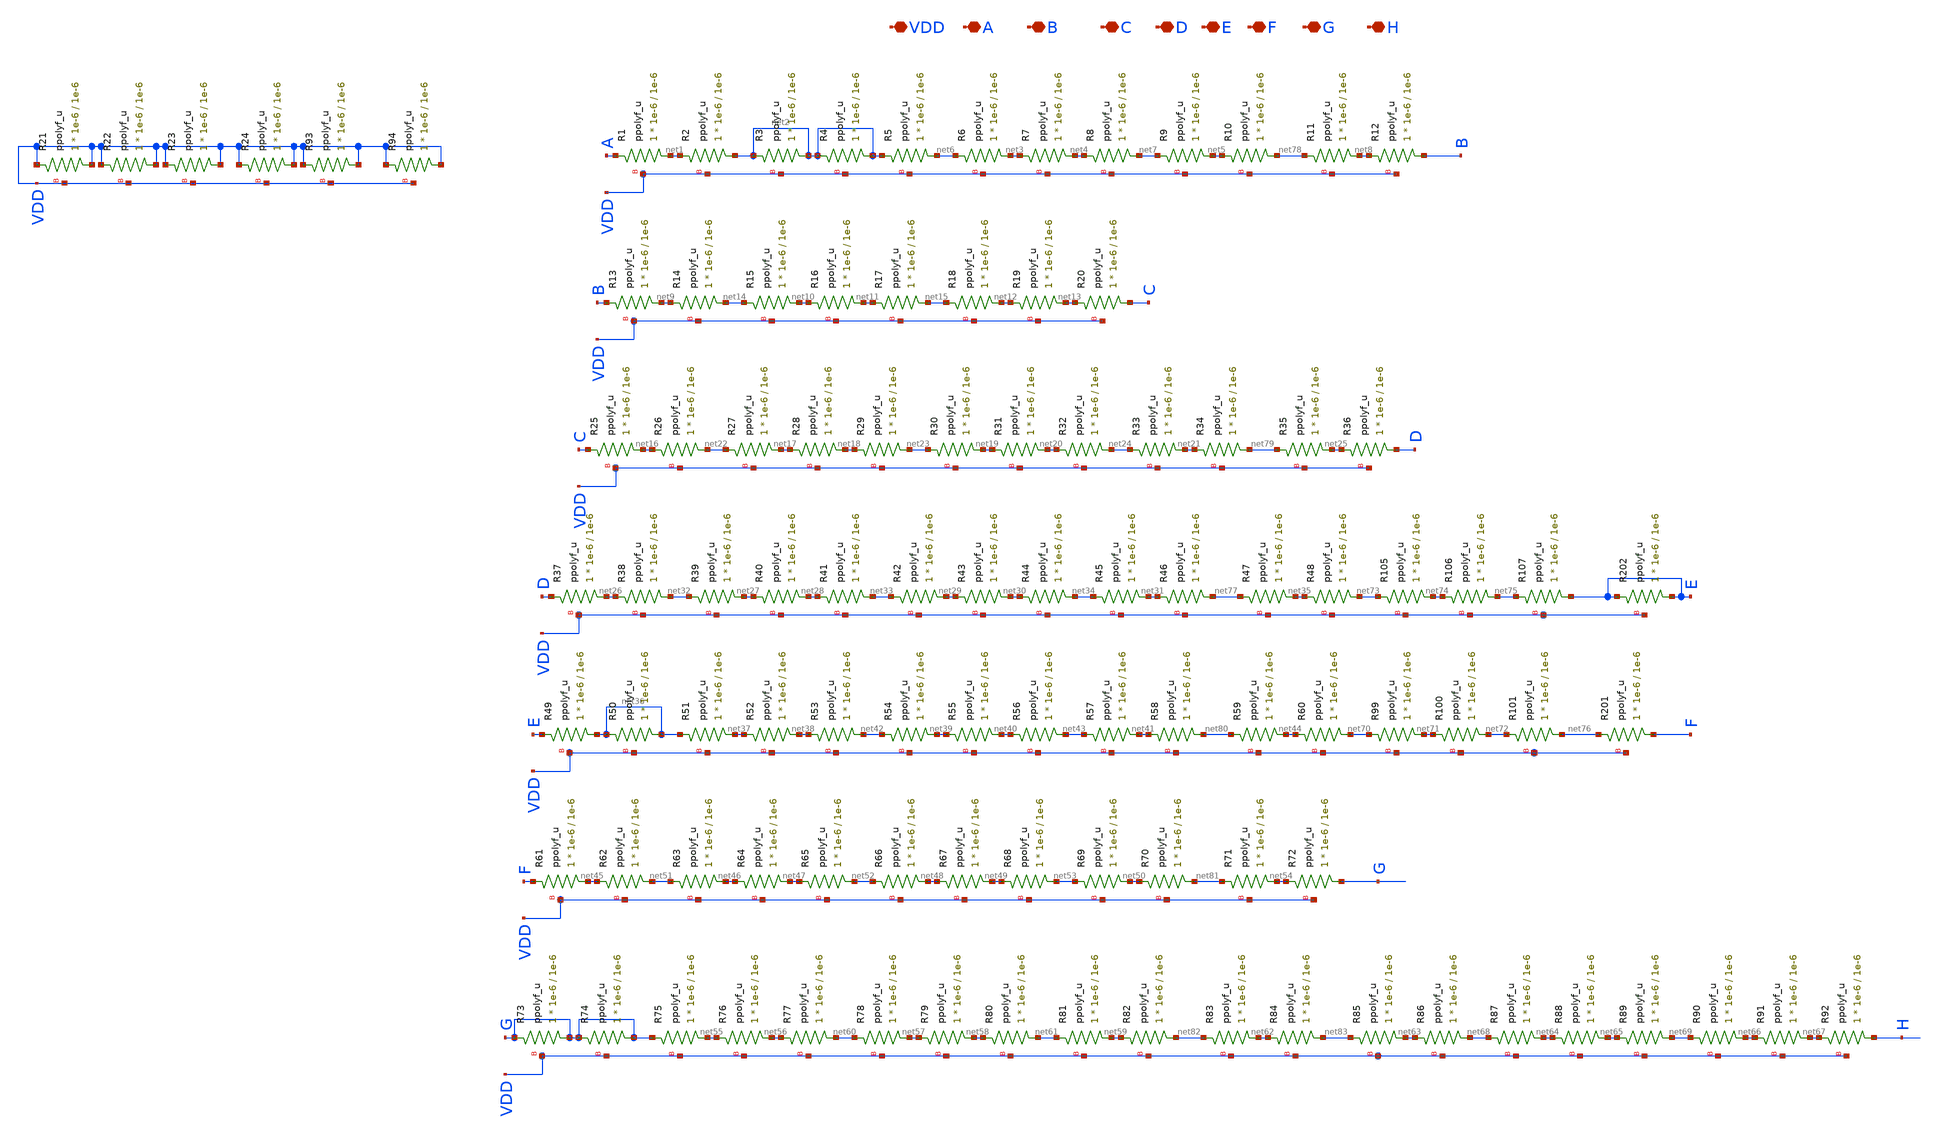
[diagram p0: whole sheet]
** sch_path: AWG_OUTPUT_AND_MUX_PAKISTAN_05/xschem/res_pga1.sch
**.subckt res_pga1 VDD A B C D E F G H
*.iopin VDD
*.iopin A
*.iopin B
*.iopin C
*.iopin D
*.iopin E
*.iopin F
*.iopin G
*.iopin H
XR1 net1 A VDD ppolyf_u r_width=1e-6 r_length=1e-6 m=1
XR2 net2 net1 VDD ppolyf_u r_width=1e-6 r_length=1e-6 m=1
XR3 net2 net2 VDD ppolyf_u r_width=1e-6 r_length=1e-6 m=1
XR4 net2 net2 VDD ppolyf_u r_width=1e-6 r_length=1e-6 m=1
XR5 net6 net2 VDD ppolyf_u r_width=1e-6 r_length=1e-6 m=1
XR6 net3 net6 VDD ppolyf_u r_width=1e-6 r_length=1e-6 m=1
XR7 net4 net3 VDD ppolyf_u r_width=1e-6 r_length=1e-6 m=1
XR8 net7 net4 VDD ppolyf_u r_width=1e-6 r_length=1e-6 m=1
XR9 net5 net7 VDD ppolyf_u r_width=1e-6 r_length=1e-6 m=1
XR10 net78 net5 VDD ppolyf_u r_width=1e-6 r_length=1e-6 m=1
XR11 net8 net78 VDD ppolyf_u r_width=1e-6 r_length=1e-6 m=1
XR12 B net8 VDD ppolyf_u r_width=1e-6 r_length=1e-6 m=1
XR13 net9 B VDD ppolyf_u r_width=1e-6 r_length=1e-6 m=1
XR14 net14 net9 VDD ppolyf_u r_width=1e-6 r_length=1e-6 m=1
XR15 net10 net14 VDD ppolyf_u r_width=1e-6 r_length=1e-6 m=1
XR16 net11 net10 VDD ppolyf_u r_width=1e-6 r_length=1e-6 m=1
XR17 net15 net11 VDD ppolyf_u r_width=1e-6 r_length=1e-6 m=1
XR18 net12 net15 VDD ppolyf_u r_width=1e-6 r_length=1e-6 m=1
XR19 net13 net12 VDD ppolyf_u r_width=1e-6 r_length=1e-6 m=1
XR20 C net13 VDD ppolyf_u r_width=1e-6 r_length=1e-6 m=1
XR25 net16 C VDD ppolyf_u r_width=1e-6 r_length=1e-6 m=1
XR26 net22 net16 VDD ppolyf_u r_width=1e-6 r_length=1e-6 m=1
XR27 net17 net22 VDD ppolyf_u r_width=1e-6 r_length=1e-6 m=1
XR28 net18 net17 VDD ppolyf_u r_width=1e-6 r_length=1e-6 m=1
XR29 net23 net18 VDD ppolyf_u r_width=1e-6 r_length=1e-6 m=1
XR30 net19 net23 VDD ppolyf_u r_width=1e-6 r_length=1e-6 m=1
XR31 net20 net19 VDD ppolyf_u r_width=1e-6 r_length=1e-6 m=1
XR32 net24 net20 VDD ppolyf_u r_width=1e-6 r_length=1e-6 m=1
XR33 net21 net24 VDD ppolyf_u r_width=1e-6 r_length=1e-6 m=1
XR34 net79 net21 VDD ppolyf_u r_width=1e-6 r_length=1e-6 m=1
XR35 net25 net79 VDD ppolyf_u r_width=1e-6 r_length=1e-6 m=1
XR36 D net25 VDD ppolyf_u r_width=1e-6 r_length=1e-6 m=1
XR37 net26 D VDD ppolyf_u r_width=1e-6 r_length=1e-6 m=1
XR38 net32 net26 VDD ppolyf_u r_width=1e-6 r_length=1e-6 m=1
XR39 net27 net32 VDD ppolyf_u r_width=1e-6 r_length=1e-6 m=1
XR40 net28 net27 VDD ppolyf_u r_width=1e-6 r_length=1e-6 m=1
XR41 net33 net28 VDD ppolyf_u r_width=1e-6 r_length=1e-6 m=1
XR42 net29 net33 VDD ppolyf_u r_width=1e-6 r_length=1e-6 m=1
XR43 net30 net29 VDD ppolyf_u r_width=1e-6 r_length=1e-6 m=1
XR44 net34 net30 VDD ppolyf_u r_width=1e-6 r_length=1e-6 m=1
XR45 net31 net34 VDD ppolyf_u r_width=1e-6 r_length=1e-6 m=1
XR46 net77 net31 VDD ppolyf_u r_width=1e-6 r_length=1e-6 m=1
XR47 net35 net77 VDD ppolyf_u r_width=1e-6 r_length=1e-6 m=1
XR48 net73 net35 VDD ppolyf_u r_width=1e-6 r_length=1e-6 m=1
XR49 net36 E VDD ppolyf_u r_width=1e-6 r_length=1e-6 m=1
XR50 net36 net36 VDD ppolyf_u r_width=1e-6 r_length=1e-6 m=1
XR51 net37 net36 VDD ppolyf_u r_width=1e-6 r_length=1e-6 m=1
XR52 net38 net37 VDD ppolyf_u r_width=1e-6 r_length=1e-6 m=1
XR53 net42 net38 VDD ppolyf_u r_width=1e-6 r_length=1e-6 m=1
XR54 net39 net42 VDD ppolyf_u r_width=1e-6 r_length=1e-6 m=1
XR55 net40 net39 VDD ppolyf_u r_width=1e-6 r_length=1e-6 m=1
XR56 net43 net40 VDD ppolyf_u r_width=1e-6 r_length=1e-6 m=1
XR57 net41 net43 VDD ppolyf_u r_width=1e-6 r_length=1e-6 m=1
XR58 net80 net41 VDD ppolyf_u r_width=1e-6 r_length=1e-6 m=1
XR59 net44 net80 VDD ppolyf_u r_width=1e-6 r_length=1e-6 m=1
XR60 net70 net44 VDD ppolyf_u r_width=1e-6 r_length=1e-6 m=1
XR61 net45 F VDD ppolyf_u r_width=1e-6 r_length=1e-6 m=1
XR62 net51 net45 VDD ppolyf_u r_width=1e-6 r_length=1e-6 m=1
XR63 net46 net51 VDD ppolyf_u r_width=1e-6 r_length=1e-6 m=1
XR64 net47 net46 VDD ppolyf_u r_width=1e-6 r_length=1e-6 m=1
XR65 net52 net47 VDD ppolyf_u r_width=1e-6 r_length=1e-6 m=1
XR66 net48 net52 VDD ppolyf_u r_width=1e-6 r_length=1e-6 m=1
XR67 net49 net48 VDD ppolyf_u r_width=1e-6 r_length=1e-6 m=1
XR68 net53 net49 VDD ppolyf_u r_width=1e-6 r_length=1e-6 m=1
XR69 net50 net53 VDD ppolyf_u r_width=1e-6 r_length=1e-6 m=1
XR70 net81 net50 VDD ppolyf_u r_width=1e-6 r_length=1e-6 m=1
XR71 net54 net81 VDD ppolyf_u r_width=1e-6 r_length=1e-6 m=1
XR72 G net54 VDD ppolyf_u r_width=1e-6 r_length=1e-6 m=1
XR73 G G VDD ppolyf_u r_width=1e-6 r_length=1e-6 m=1
XR74 G G VDD ppolyf_u r_width=1e-6 r_length=1e-6 m=1
XR75 net55 G VDD ppolyf_u r_width=1e-6 r_length=1e-6 m=1
XR76 net56 net55 VDD ppolyf_u r_width=1e-6 r_length=1e-6 m=1
XR77 net60 net56 VDD ppolyf_u r_width=1e-6 r_length=1e-6 m=1
XR78 net57 net60 VDD ppolyf_u r_width=1e-6 r_length=1e-6 m=1
XR79 net58 net57 VDD ppolyf_u r_width=1e-6 r_length=1e-6 m=1
XR80 net61 net58 VDD ppolyf_u r_width=1e-6 r_length=1e-6 m=1
XR81 net59 net61 VDD ppolyf_u r_width=1e-6 r_length=1e-6 m=1
XR82 net82 net59 VDD ppolyf_u r_width=1e-6 r_length=1e-6 m=1
XR83 net62 net82 VDD ppolyf_u r_width=1e-6 r_length=1e-6 m=1
XR84 net83 net62 VDD ppolyf_u r_width=1e-6 r_length=1e-6 m=1
XR85 net63 net83 VDD ppolyf_u r_width=1e-6 r_length=1e-6 m=1
XR86 net68 net63 VDD ppolyf_u r_width=1e-6 r_length=1e-6 m=1
XR87 net64 net68 VDD ppolyf_u r_width=1e-6 r_length=1e-6 m=1
XR88 net65 net64 VDD ppolyf_u r_width=1e-6 r_length=1e-6 m=1
XR89 net69 net65 VDD ppolyf_u r_width=1e-6 r_length=1e-6 m=1
XR90 net66 net69 VDD ppolyf_u r_width=1e-6 r_length=1e-6 m=1
XR91 net67 net66 VDD ppolyf_u r_width=1e-6 r_length=1e-6 m=1
XR92 H net67 VDD ppolyf_u r_width=1e-6 r_length=1e-6 m=1
XR99 net71 net70 VDD ppolyf_u r_width=1e-6 r_length=1e-6 m=1
XR100 net72 net71 VDD ppolyf_u r_width=1e-6 r_length=1e-6 m=1
XR101 net76 net72 VDD ppolyf_u r_width=1e-6 r_length=1e-6 m=1
XR105 net74 net73 VDD ppolyf_u r_width=1e-6 r_length=1e-6 m=1
XR106 net75 net74 VDD ppolyf_u r_width=1e-6 r_length=1e-6 m=1
XR107 E net75 VDD ppolyf_u r_width=1e-6 r_length=1e-6 m=1
XR21 VDD VDD VDD ppolyf_u r_width=1e-6 r_length=1e-6 m=1
XR22 VDD VDD VDD ppolyf_u r_width=1e-6 r_length=1e-6 m=1
XR23 VDD VDD VDD ppolyf_u r_width=1e-6 r_length=1e-6 m=1
XR24 VDD VDD VDD ppolyf_u r_width=1e-6 r_length=1e-6 m=1
XR93 VDD VDD VDD ppolyf_u r_width=1e-6 r_length=1e-6 m=1
XR94 VDD VDD VDD ppolyf_u r_width=1e-6 r_length=1e-6 m=1
XR201 F net76 VDD ppolyf_u r_width=1e-6 r_length=1e-6 m=1
XR202 E E VDD ppolyf_u r_width=1e-6 r_length=1e-6 m=1
**.ends
.end
